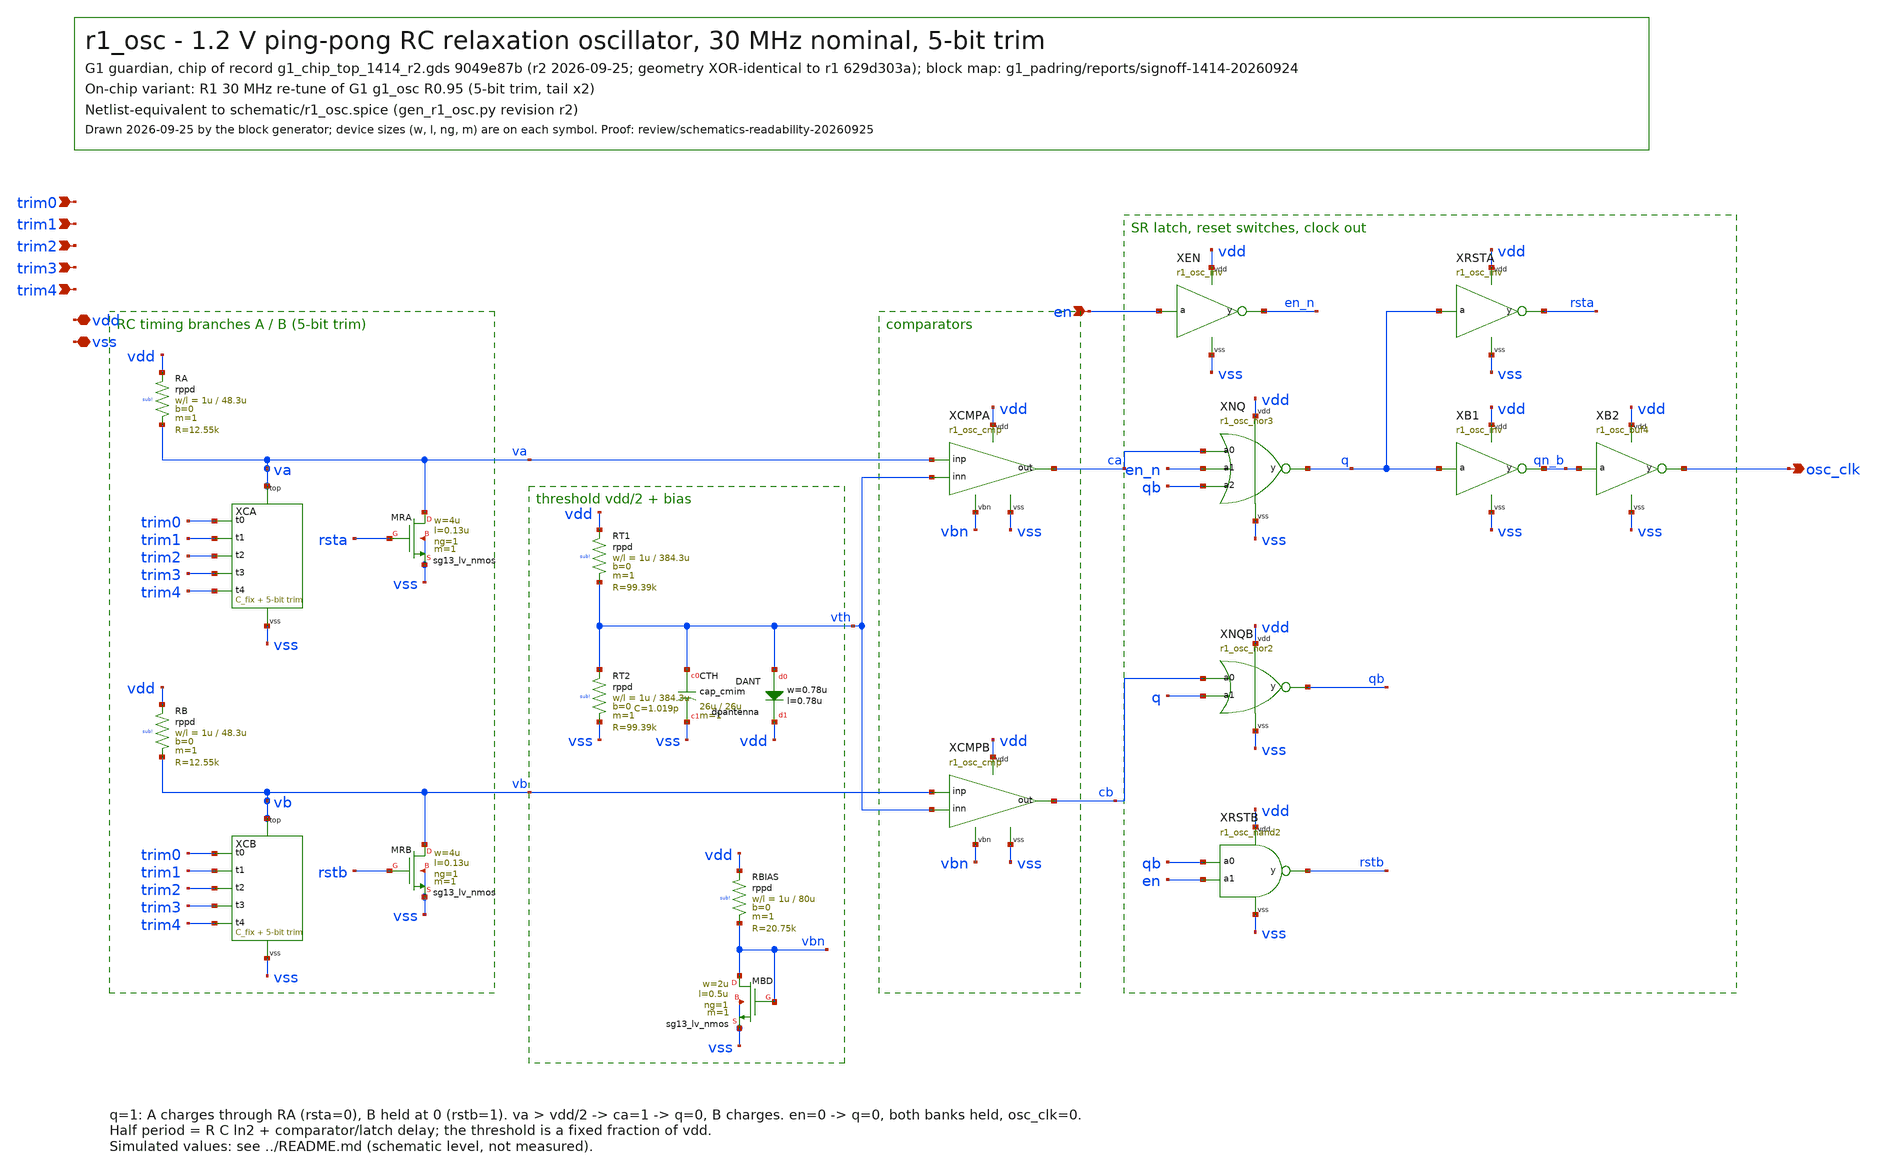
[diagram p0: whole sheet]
** sch_path: designs/r1-joint/blocks/r1_osc/schematic/r1_osc.sch
**.subckt r1_osc en trim0 trim1 trim2 trim3 trim4 osc_clk vdd vss
*.ipin en
*.ipin trim0
*.ipin trim1
*.ipin trim2
*.ipin trim3
*.ipin trim4
*.opin osc_clk
*.iopin vdd
*.iopin vss
XRA vdd va sub! rppd w=1u l=48.3u m=1 b=0 mm_ok=1
XRB vdd vb sub! rppd w=1u l=48.3u m=1 b=0 mm_ok=1
XCA trim0 trim1 trim2 trim3 trim4 va vss r1_osc_cbank
XCB trim0 trim1 trim2 trim3 trim4 vb vss r1_osc_cbank
XMRA va rsta vss vss sg13_lv_nmos w=4u l=0.13u ng=1 m=1 mm_ok=1
XMRB vb rstb vss vss sg13_lv_nmos w=4u l=0.13u ng=1 m=1 mm_ok=1
XRT1 vdd vth sub! rppd w=1u l=384.3u m=1 b=0 mm_ok=1
XRT2 vth vss sub! rppd w=1u l=384.3u m=1 b=0 mm_ok=1
XCTH vth vss cap_cmim w=26u l=26u m=1 mm_ok=1
XDANT vth vdd dpantenna l=0.78u w=0.78u
XRBIAS vdd vbn sub! rppd w=1u l=80u m=1 b=0 mm_ok=1
XMBD vbn vbn vss vss sg13_lv_nmos w=2u l=0.5u ng=1 m=1 mm_ok=1
XCMPA va vth vbn ca vdd vss r1_osc_cmp
XCMPB vb vth vbn cb vdd vss r1_osc_cmp
XEN en en_n vdd vss r1_osc_inv
XNQ ca en_n qb q vdd vss r1_osc_nor3
XNQB cb q qb vdd vss r1_osc_nor2
XRSTB qb en rstb vdd vss r1_osc_nand2
XRSTA q rsta vdd vss r1_osc_inv
XB1 q qn_b vdd vss r1_osc_inv
XB2 qn_b osc_clk vdd vss r1_osc_buf4
**.ends

* expanding   symbol:  r1_osc_cbank.sym # of pins=7
** sym_path: designs/r1-joint/blocks/r1_osc/schematic/r1_osc_cbank.sym
** sch_path: designs/r1-joint/blocks/r1_osc/schematic/r1_osc_cbank.sch
.subckt r1_osc_cbank t0 t1 t2 t3 t4 top vss
*.ipin t0
*.ipin t1
*.ipin t2
*.ipin t3
*.ipin t4
*.iopin top
*.iopin vss
XCF top vss cap_cmim w=26.70u l=26.70u m=1 mm_ok=1
XCT0 top b0 cap_cmim w=4.03u l=4.03u m=1 mm_ok=1
XMS0 b0 t0 vss vss sg13_lv_nmos w=0.5u l=0.13u ng=1 m=1 mm_ok=1
XCT1 top b1 cap_cmim w=4.03u l=4.03u m=2 mm_ok=1
XMS1 b1 t1 vss vss sg13_lv_nmos w=0.5u l=0.13u ng=1 m=1 mm_ok=1
XCT2 top b2 cap_cmim w=4.03u l=4.03u m=4 mm_ok=1
XMS2 b2 t2 vss vss sg13_lv_nmos w=1u l=0.13u ng=1 m=1 mm_ok=1
XCT3 top b3 cap_cmim w=4.03u l=4.03u m=8 mm_ok=1
XMS3 b3 t3 vss vss sg13_lv_nmos w=2u l=0.13u ng=1 m=1 mm_ok=1
XCT4 top b4 cap_cmim w=4.03u l=4.03u m=16 mm_ok=1
XMS4 b4 t4 vss vss sg13_lv_nmos w=4u l=0.13u ng=1 m=1 mm_ok=1
.ends


* expanding   symbol:  r1_osc_cmp.sym # of pins=6
** sym_path: designs/r1-joint/blocks/r1_osc/schematic/r1_osc_cmp.sym
** sch_path: designs/r1-joint/blocks/r1_osc/schematic/r1_osc_cmp.sch
.subckt r1_osc_cmp inp inn vbn out vdd vss
*.ipin inp
*.ipin inn
*.ipin vbn
*.opin out
*.iopin vdd
*.iopin vss
XMT tail vbn vss vss sg13_lv_nmos w=2u l=0.5u ng=1 m=2 mm_ok=1
XM1 d1 inp tail vss sg13_lv_nmos w=4u l=0.3u ng=1 m=1 mm_ok=1
XM2 o1 inn tail vss sg13_lv_nmos w=4u l=0.3u ng=1 m=1 mm_ok=1
XM3 d1 d1 vdd vdd sg13_lv_pmos w=2u l=0.3u ng=1 m=1 mm_ok=1
XM4 o1 d1 vdd vdd sg13_lv_pmos w=2u l=0.3u ng=1 m=1 mm_ok=1
XI1 o1 o2 vdd vss r1_osc_inv
XI2 o2 out vdd vss r1_osc_inv
.ends


* expanding   symbol:  r1_osc_inv.sym # of pins=4
** sym_path: designs/r1-joint/blocks/r1_osc/schematic/r1_osc_inv.sym
** sch_path: designs/r1-joint/blocks/r1_osc/schematic/r1_osc_inv.sch
.subckt r1_osc_inv a y vdd vss
*.ipin a
*.opin y
*.iopin vdd
*.iopin vss
XMP y a vdd vdd sg13_lv_pmos w=1u l=0.13u ng=1 m=1 mm_ok=1
XMN y a vss vss sg13_lv_nmos w=0.5u l=0.13u ng=1 m=1 mm_ok=1
.ends


* expanding   symbol:  r1_osc_nor3.sym # of pins=6
** sym_path: designs/r1-joint/blocks/r1_osc/schematic/r1_osc_nor3.sym
** sch_path: designs/r1-joint/blocks/r1_osc/schematic/r1_osc_nor3.sch
.subckt r1_osc_nor3 a0 a1 a2 y vdd vss
*.ipin a0
*.ipin a1
*.ipin a2
*.opin y
*.iopin vdd
*.iopin vss
XMP0 p0 a0 vdd vdd sg13_lv_pmos w=3u l=0.13u ng=1 m=1 mm_ok=1
XMP1 p1 a1 p0 vdd sg13_lv_pmos w=3u l=0.13u ng=1 m=1 mm_ok=1
XMP2 y a2 p1 vdd sg13_lv_pmos w=3u l=0.13u ng=1 m=1 mm_ok=1
XMN0 y a0 vss vss sg13_lv_nmos w=0.5u l=0.13u ng=1 m=1 mm_ok=1
XMN1 y a1 vss vss sg13_lv_nmos w=0.5u l=0.13u ng=1 m=1 mm_ok=1
XMN2 y a2 vss vss sg13_lv_nmos w=0.5u l=0.13u ng=1 m=1 mm_ok=1
.ends


* expanding   symbol:  r1_osc_nor2.sym # of pins=5
** sym_path: designs/r1-joint/blocks/r1_osc/schematic/r1_osc_nor2.sym
** sch_path: designs/r1-joint/blocks/r1_osc/schematic/r1_osc_nor2.sch
.subckt r1_osc_nor2 a0 a1 y vdd vss
*.ipin a0
*.ipin a1
*.opin y
*.iopin vdd
*.iopin vss
XMP0 p0 a0 vdd vdd sg13_lv_pmos w=2u l=0.13u ng=1 m=1 mm_ok=1
XMP1 y a1 p0 vdd sg13_lv_pmos w=2u l=0.13u ng=1 m=1 mm_ok=1
XMN0 y a0 vss vss sg13_lv_nmos w=0.5u l=0.13u ng=1 m=1 mm_ok=1
XMN1 y a1 vss vss sg13_lv_nmos w=0.5u l=0.13u ng=1 m=1 mm_ok=1
.ends


* expanding   symbol:  r1_osc_nand2.sym # of pins=5
** sym_path: designs/r1-joint/blocks/r1_osc/schematic/r1_osc_nand2.sym
** sch_path: designs/r1-joint/blocks/r1_osc/schematic/r1_osc_nand2.sch
.subckt r1_osc_nand2 a0 a1 y vdd vss
*.ipin a0
*.ipin a1
*.opin y
*.iopin vdd
*.iopin vss
XMP0 y a0 vdd vdd sg13_lv_pmos w=1u l=0.13u ng=1 m=1 mm_ok=1
XMP1 y a1 vdd vdd sg13_lv_pmos w=1u l=0.13u ng=1 m=1 mm_ok=1
XMN0 y a0 n0 vss sg13_lv_nmos w=1u l=0.13u ng=1 m=1 mm_ok=1
XMN1 n0 a1 vss vss sg13_lv_nmos w=1u l=0.13u ng=1 m=1 mm_ok=1
.ends


* expanding   symbol:  r1_osc_buf4.sym # of pins=4
** sym_path: designs/r1-joint/blocks/r1_osc/schematic/r1_osc_buf4.sym
** sch_path: designs/r1-joint/blocks/r1_osc/schematic/r1_osc_buf4.sch
.subckt r1_osc_buf4 a y vdd vss
*.ipin a
*.opin y
*.iopin vdd
*.iopin vss
XMP y a vdd vdd sg13_lv_pmos w=4u l=0.13u ng=1 m=1 mm_ok=1
XMN y a vss vss sg13_lv_nmos w=2u l=0.13u ng=1 m=1 mm_ok=1
.ends

.end
